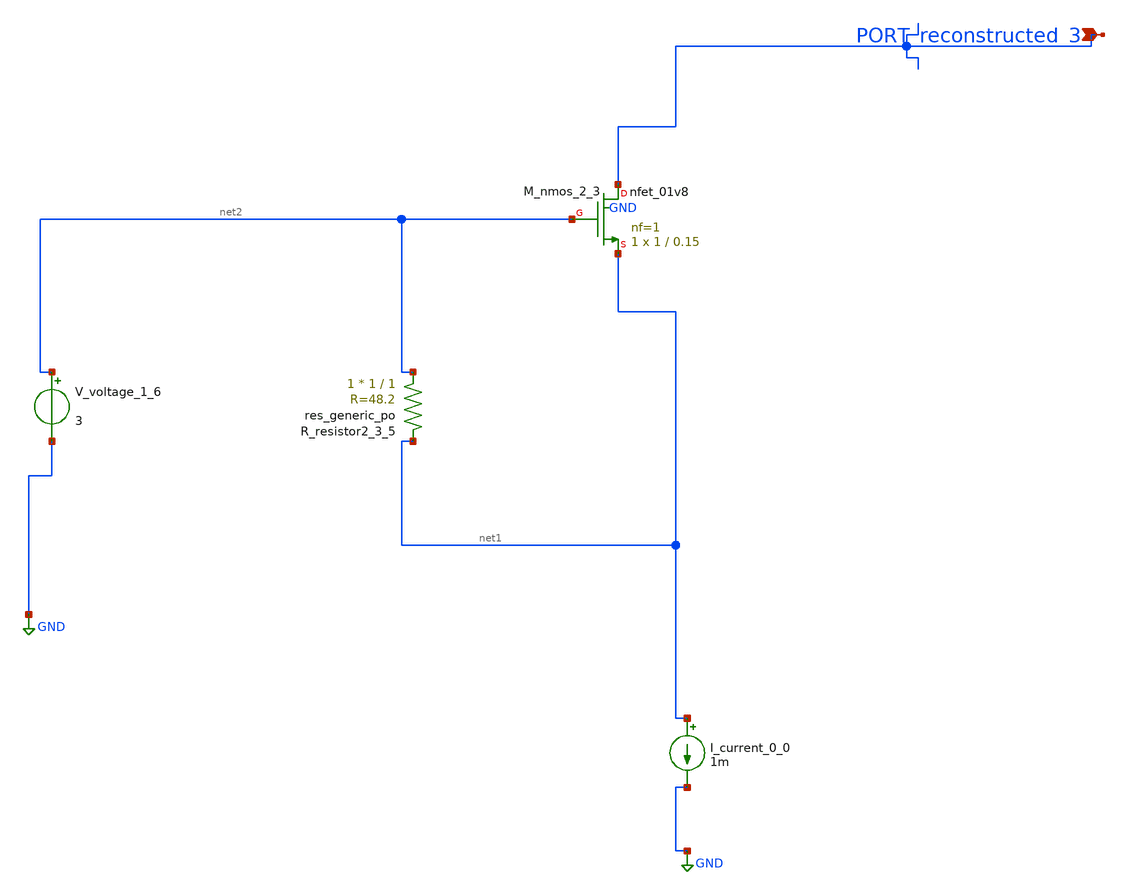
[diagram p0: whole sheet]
** sch_path: schematics/AMSNet/32.sch
**.subckt 32 PORT_reconstructed_3
*.ipin PORT_reconstructed_3
I_current_0_0 net1 GND 1m
XM_nmos_2_3 PORT_reconstructed_3 net2 net1 GND sky130_fd_pr__nfet_01v8 L=0.15 W=1 nf=1 ad='int((1 + 1)/2) * 1 / 1 * 0.29'
+ as='int((1 + 2)/2) * 1 / 1 * 0.29' pd='2*int((1 + 1)/2) * (1 / 1 + 0.29)' ps='2*int((1 + 2)/2) * (1 / 1 + 0.29)'
+ nrd='0.29 / 1 ' nrs='0.29 / 1 ' sa=0 sb=0 sd=0 mult=1 m=1
XR_resistor2_3_5 net2 net1 sky130_fd_pr__res_generic_po W=1 L=1 m=1
V_voltage_1_6 net2 GND 3
**.ends
.GLOBAL GND
.end
